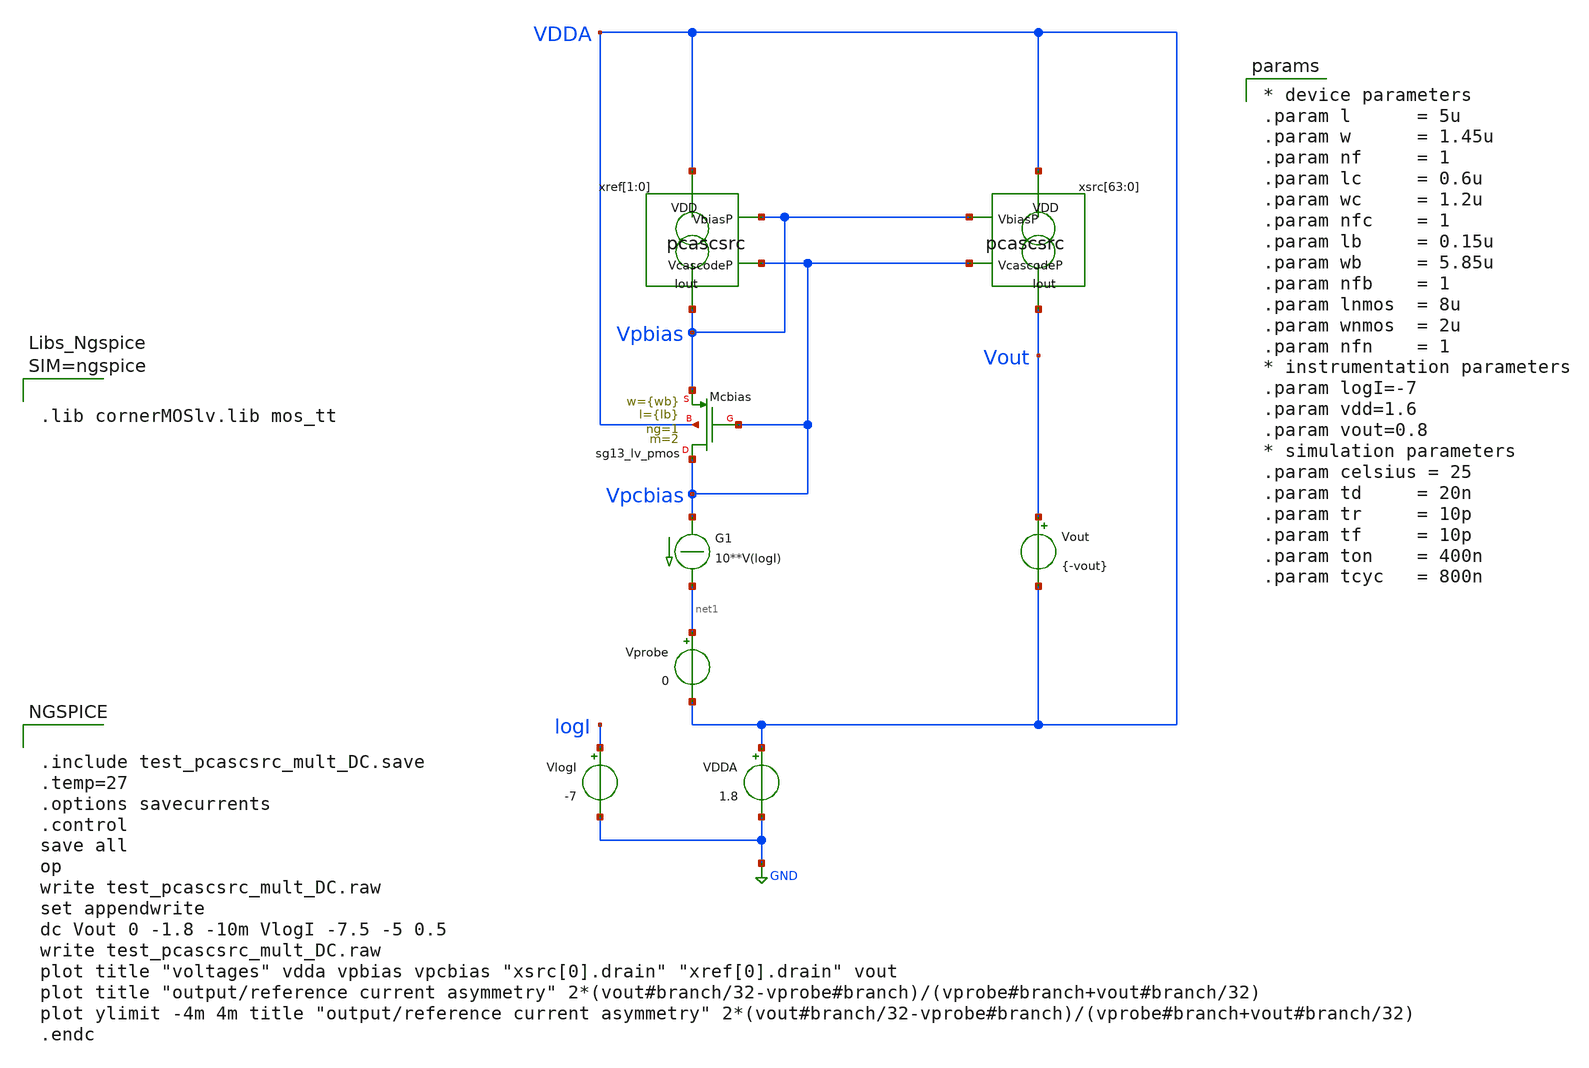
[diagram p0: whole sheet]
** sch_path: xschem/test_pcascsrc_mult_DC.sch
**.subckt test_pcascsrc_mult_DC
Vout Vout VDDA {-vout}
.save i(vout)
Vprobe net1 VDDA 0
.save i(vprobe)
G1 Vpcbias net1 CUR=' 10**V(logI) '
VlogI logI GND -7
.save i(vlogi)
xref[1] VDDA Vpbias Vpcbias Vpbias pcascsrc l={l} w={w} lc={lc} wc={wc}
xref[0] VDDA Vpbias Vpcbias Vpbias pcascsrc l={l} w={w} lc={lc} wc={wc}
xsrc[63] VDDA Vpbias Vpcbias Vout pcascsrc l={l} w={w} lc={lc} wc={wc}
xsrc[62] VDDA Vpbias Vpcbias Vout pcascsrc l={l} w={w} lc={lc} wc={wc}
xsrc[61] VDDA Vpbias Vpcbias Vout pcascsrc l={l} w={w} lc={lc} wc={wc}
xsrc[60] VDDA Vpbias Vpcbias Vout pcascsrc l={l} w={w} lc={lc} wc={wc}
xsrc[59] VDDA Vpbias Vpcbias Vout pcascsrc l={l} w={w} lc={lc} wc={wc}
xsrc[58] VDDA Vpbias Vpcbias Vout pcascsrc l={l} w={w} lc={lc} wc={wc}
xsrc[57] VDDA Vpbias Vpcbias Vout pcascsrc l={l} w={w} lc={lc} wc={wc}
xsrc[56] VDDA Vpbias Vpcbias Vout pcascsrc l={l} w={w} lc={lc} wc={wc}
xsrc[55] VDDA Vpbias Vpcbias Vout pcascsrc l={l} w={w} lc={lc} wc={wc}
xsrc[54] VDDA Vpbias Vpcbias Vout pcascsrc l={l} w={w} lc={lc} wc={wc}
xsrc[53] VDDA Vpbias Vpcbias Vout pcascsrc l={l} w={w} lc={lc} wc={wc}
xsrc[52] VDDA Vpbias Vpcbias Vout pcascsrc l={l} w={w} lc={lc} wc={wc}
xsrc[51] VDDA Vpbias Vpcbias Vout pcascsrc l={l} w={w} lc={lc} wc={wc}
xsrc[50] VDDA Vpbias Vpcbias Vout pcascsrc l={l} w={w} lc={lc} wc={wc}
xsrc[49] VDDA Vpbias Vpcbias Vout pcascsrc l={l} w={w} lc={lc} wc={wc}
xsrc[48] VDDA Vpbias Vpcbias Vout pcascsrc l={l} w={w} lc={lc} wc={wc}
xsrc[47] VDDA Vpbias Vpcbias Vout pcascsrc l={l} w={w} lc={lc} wc={wc}
xsrc[46] VDDA Vpbias Vpcbias Vout pcascsrc l={l} w={w} lc={lc} wc={wc}
xsrc[45] VDDA Vpbias Vpcbias Vout pcascsrc l={l} w={w} lc={lc} wc={wc}
xsrc[44] VDDA Vpbias Vpcbias Vout pcascsrc l={l} w={w} lc={lc} wc={wc}
xsrc[43] VDDA Vpbias Vpcbias Vout pcascsrc l={l} w={w} lc={lc} wc={wc}
xsrc[42] VDDA Vpbias Vpcbias Vout pcascsrc l={l} w={w} lc={lc} wc={wc}
xsrc[41] VDDA Vpbias Vpcbias Vout pcascsrc l={l} w={w} lc={lc} wc={wc}
xsrc[40] VDDA Vpbias Vpcbias Vout pcascsrc l={l} w={w} lc={lc} wc={wc}
xsrc[39] VDDA Vpbias Vpcbias Vout pcascsrc l={l} w={w} lc={lc} wc={wc}
xsrc[38] VDDA Vpbias Vpcbias Vout pcascsrc l={l} w={w} lc={lc} wc={wc}
xsrc[37] VDDA Vpbias Vpcbias Vout pcascsrc l={l} w={w} lc={lc} wc={wc}
xsrc[36] VDDA Vpbias Vpcbias Vout pcascsrc l={l} w={w} lc={lc} wc={wc}
xsrc[35] VDDA Vpbias Vpcbias Vout pcascsrc l={l} w={w} lc={lc} wc={wc}
xsrc[34] VDDA Vpbias Vpcbias Vout pcascsrc l={l} w={w} lc={lc} wc={wc}
xsrc[33] VDDA Vpbias Vpcbias Vout pcascsrc l={l} w={w} lc={lc} wc={wc}
xsrc[32] VDDA Vpbias Vpcbias Vout pcascsrc l={l} w={w} lc={lc} wc={wc}
xsrc[31] VDDA Vpbias Vpcbias Vout pcascsrc l={l} w={w} lc={lc} wc={wc}
xsrc[30] VDDA Vpbias Vpcbias Vout pcascsrc l={l} w={w} lc={lc} wc={wc}
xsrc[29] VDDA Vpbias Vpcbias Vout pcascsrc l={l} w={w} lc={lc} wc={wc}
xsrc[28] VDDA Vpbias Vpcbias Vout pcascsrc l={l} w={w} lc={lc} wc={wc}
xsrc[27] VDDA Vpbias Vpcbias Vout pcascsrc l={l} w={w} lc={lc} wc={wc}
xsrc[26] VDDA Vpbias Vpcbias Vout pcascsrc l={l} w={w} lc={lc} wc={wc}
xsrc[25] VDDA Vpbias Vpcbias Vout pcascsrc l={l} w={w} lc={lc} wc={wc}
xsrc[24] VDDA Vpbias Vpcbias Vout pcascsrc l={l} w={w} lc={lc} wc={wc}
xsrc[23] VDDA Vpbias Vpcbias Vout pcascsrc l={l} w={w} lc={lc} wc={wc}
xsrc[22] VDDA Vpbias Vpcbias Vout pcascsrc l={l} w={w} lc={lc} wc={wc}
xsrc[21] VDDA Vpbias Vpcbias Vout pcascsrc l={l} w={w} lc={lc} wc={wc}
xsrc[20] VDDA Vpbias Vpcbias Vout pcascsrc l={l} w={w} lc={lc} wc={wc}
xsrc[19] VDDA Vpbias Vpcbias Vout pcascsrc l={l} w={w} lc={lc} wc={wc}
xsrc[18] VDDA Vpbias Vpcbias Vout pcascsrc l={l} w={w} lc={lc} wc={wc}
xsrc[17] VDDA Vpbias Vpcbias Vout pcascsrc l={l} w={w} lc={lc} wc={wc}
xsrc[16] VDDA Vpbias Vpcbias Vout pcascsrc l={l} w={w} lc={lc} wc={wc}
xsrc[15] VDDA Vpbias Vpcbias Vout pcascsrc l={l} w={w} lc={lc} wc={wc}
xsrc[14] VDDA Vpbias Vpcbias Vout pcascsrc l={l} w={w} lc={lc} wc={wc}
xsrc[13] VDDA Vpbias Vpcbias Vout pcascsrc l={l} w={w} lc={lc} wc={wc}
xsrc[12] VDDA Vpbias Vpcbias Vout pcascsrc l={l} w={w} lc={lc} wc={wc}
xsrc[11] VDDA Vpbias Vpcbias Vout pcascsrc l={l} w={w} lc={lc} wc={wc}
xsrc[10] VDDA Vpbias Vpcbias Vout pcascsrc l={l} w={w} lc={lc} wc={wc}
xsrc[9] VDDA Vpbias Vpcbias Vout pcascsrc l={l} w={w} lc={lc} wc={wc}
xsrc[8] VDDA Vpbias Vpcbias Vout pcascsrc l={l} w={w} lc={lc} wc={wc}
xsrc[7] VDDA Vpbias Vpcbias Vout pcascsrc l={l} w={w} lc={lc} wc={wc}
xsrc[6] VDDA Vpbias Vpcbias Vout pcascsrc l={l} w={w} lc={lc} wc={wc}
xsrc[5] VDDA Vpbias Vpcbias Vout pcascsrc l={l} w={w} lc={lc} wc={wc}
xsrc[4] VDDA Vpbias Vpcbias Vout pcascsrc l={l} w={w} lc={lc} wc={wc}
xsrc[3] VDDA Vpbias Vpcbias Vout pcascsrc l={l} w={w} lc={lc} wc={wc}
xsrc[2] VDDA Vpbias Vpcbias Vout pcascsrc l={l} w={w} lc={lc} wc={wc}
xsrc[1] VDDA Vpbias Vpcbias Vout pcascsrc l={l} w={w} lc={lc} wc={wc}
xsrc[0] VDDA Vpbias Vpcbias Vout pcascsrc l={l} w={w} lc={lc} wc={wc}
VDDA VDDA GND 1.8
.save i(vdda)
XMcbias Vpcbias Vpcbias Vpbias VDDA sg13_lv_pmos w={wb} l={lb} ng=1 m=2 mm_ok=1
**** begin user architecture code


.include test_pcascsrc_mult_DC.save
.temp=27
.options savecurrents
.control
save all
op
write test_pcascsrc_mult_DC.raw
set appendwrite
dc Vout 0 -1.8 -10m VlogI -7.5 -5 0.5
write test_pcascsrc_mult_DC.raw
plot title "voltages" vdda vpbias vpcbias "xsrc[0].drain" "xref[0].drain" vout
plot title "output/reference current asymmetry"
+ 2*(vout#branch/32-vprobe#branch)/(vprobe#branch+vout#branch/32)
plot ylimit -4m 4m title "output/reference current asymmetry"
+ 2*(vout#branch/32-vprobe#branch)/(vprobe#branch+vout#branch/32)
.endc





.lib cornerMOSlv.lib mos_tt




* device parameters
.param l      = 5u
.param w      = 1.45u
.param nf     = 1
.param lc     = 0.6u
.param wc     = 1.2u
.param nfc    = 1
.param lb     = 0.15u
.param wb     = 5.85u
.param nfb    = 1
.param lnmos  = 8u
.param wnmos  = 2u
.param nfn    = 1
* instrumentation parameters
.param logI=-7
.param vdd=1.6
.param vout=0.8
* simulation parameters
.param celsius = 25
.param td     = 20n
.param tr     = 10p
.param tf     = 10p
.param ton    = 400n
.param tcyc   = 800n


**** end user architecture code
**.ends

* expanding   symbol:  pcascsrc.sym # of pins=4
** sym_path: xschem/pcascsrc.sym
** sch_path: xschem/pcascsrc.sch
.subckt pcascsrc VDD VbiasP VcascodeP Iout  l=2u w=.74u lc=.3u wc=.3u
*.ipin VcascodeP
*.ipin VbiasP
*.opin Iout
*.ipin VDD
XMsrc drain VbiasP VDD VDD sg13_lv_pmos w={w} l={l} ng=1 m=1 mm_ok=1
XMcasc Iout VcascodeP drain VDD sg13_lv_pmos w={wc} l={lc} ng=1 m=1 mm_ok=1
.ends

.GLOBAL GND
.end
